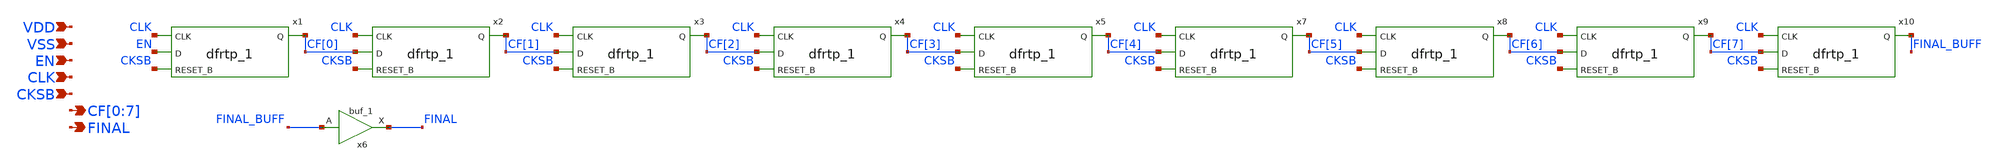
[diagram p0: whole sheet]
** sch_path: xschem/cyclic_flag.sch
**.subckt cyclic_flag VDD VSS CLK CKSB CF[0],CF[1],CF[2],CF[3],CF[4],CF[5],CF[6],CF[7] FINAL EN
*.ipin VDD
*.ipin VSS
*.ipin CLK
*.ipin CKSB
*.opin CF[0],CF[1],CF[2],CF[3],CF[4],CF[5],CF[6],CF[7]
*.opin FINAL
*.ipin EN
x1 CLK EN CKSB VSS VSS VDD VDD CF[0] sky130_fd_sc_hd__dfrtp_1
x2 CLK CF[0] CKSB VSS VSS VDD VDD CF[1] sky130_fd_sc_hd__dfrtp_1
x3 CLK CF[1] CKSB VSS VSS VDD VDD CF[2] sky130_fd_sc_hd__dfrtp_1
x4 CLK CF[2] CKSB VSS VSS VDD VDD CF[3] sky130_fd_sc_hd__dfrtp_1
x5 CLK CF[3] CKSB VSS VSS VDD VDD CF[4] sky130_fd_sc_hd__dfrtp_1
x6 FINAL_BUFF VSS VSS VDD VDD FINAL sky130_fd_sc_hd__buf_1
x7 CLK CF[4] CKSB VSS VSS VDD VDD CF[5] sky130_fd_sc_hd__dfrtp_1
x8 CLK CF[5] CKSB VSS VSS VDD VDD CF[6] sky130_fd_sc_hd__dfrtp_1
x9 CLK CF[6] CKSB VSS VSS VDD VDD CF[7] sky130_fd_sc_hd__dfrtp_1
x10 CLK CF[7] CKSB VSS VSS VDD VDD FINAL_BUFF sky130_fd_sc_hd__dfrtp_1
**.ends
.end
